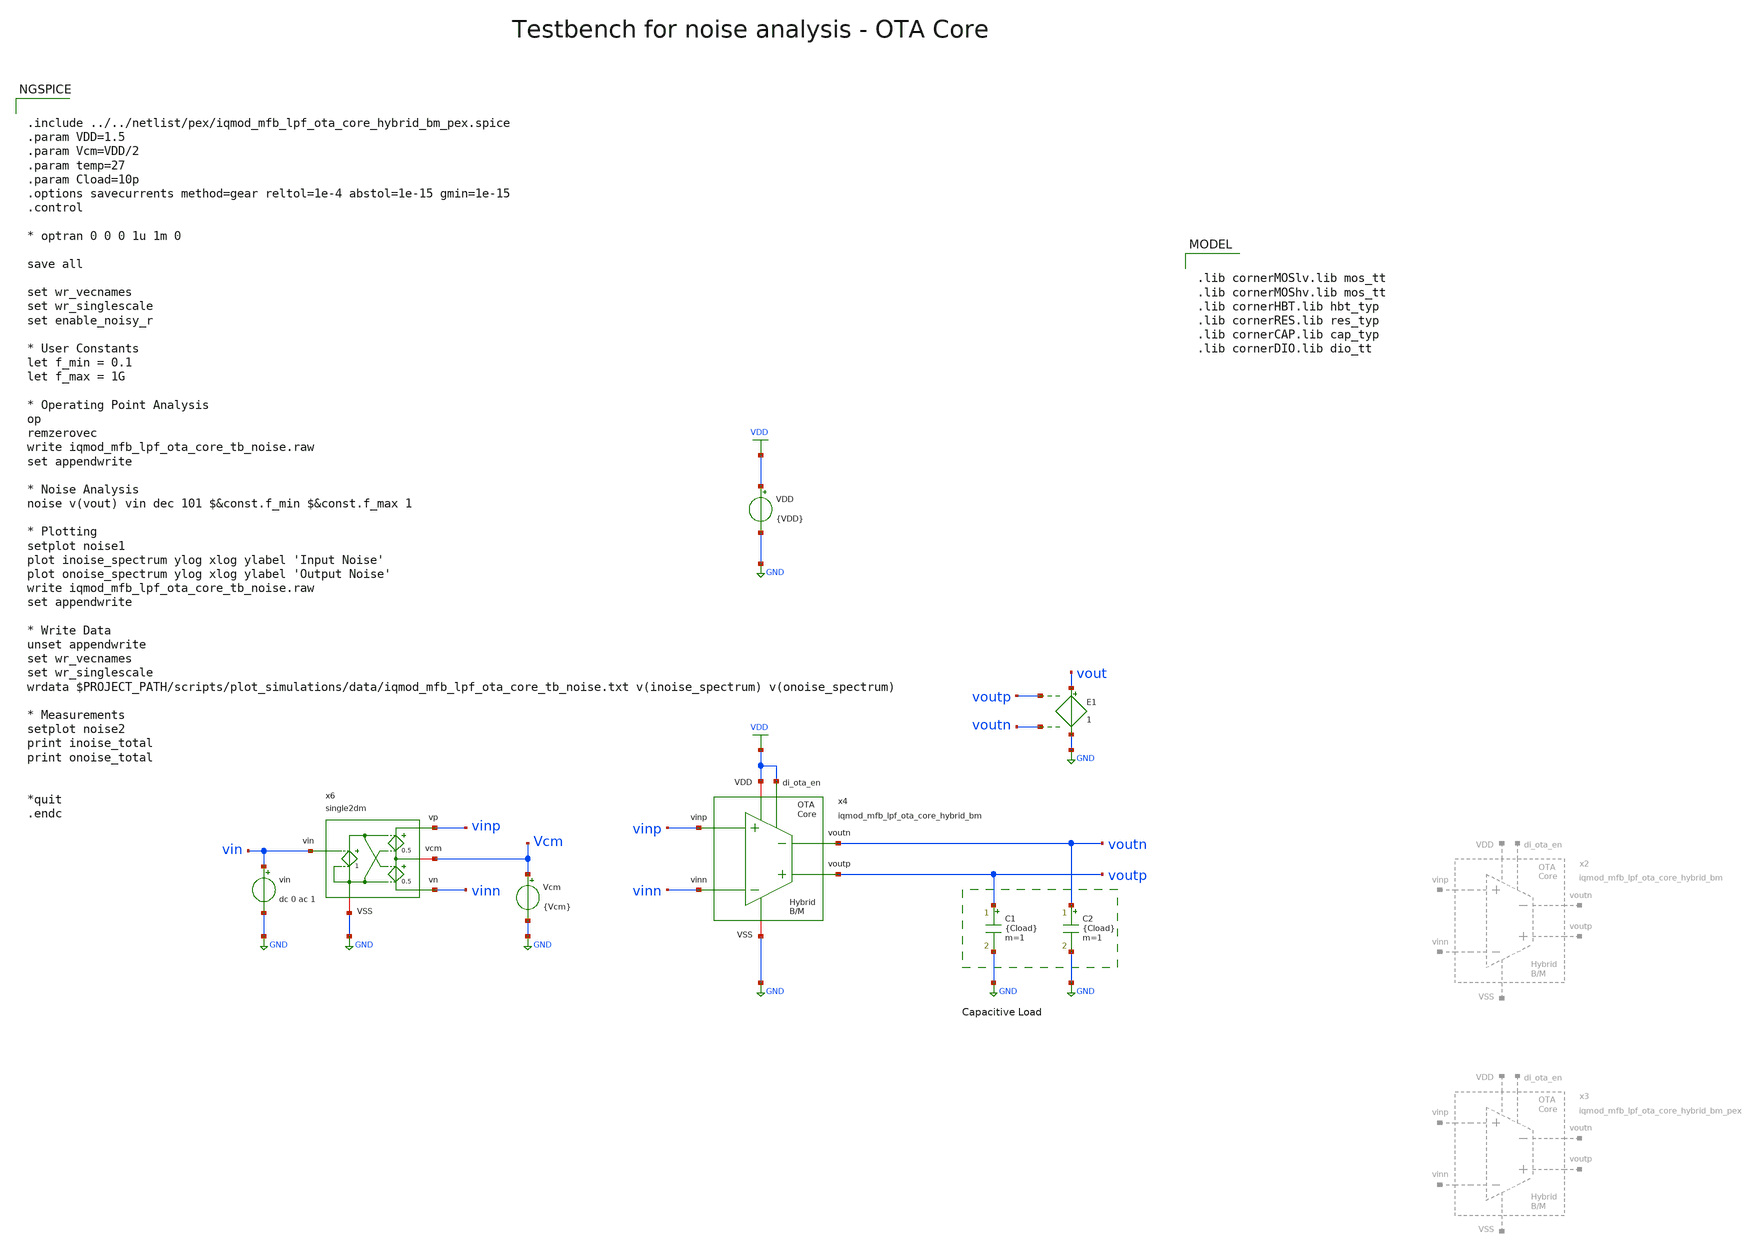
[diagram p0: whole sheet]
** sch_path: ihp130/macros/iqmod/testbenches/iqmod_mfb_lpf_ota_core_tb_noise.sch
**.subckt iqmod_mfb_lpf_ota_core_tb_noise
VDD VDD GND {VDD}
C1 voutp GND {Cload} m=1
C2 voutn GND {Cload} m=1
Vcm Vcm GND {Vcm}
E1 vout GND voutp voutn 1
vin vin GND dc 0 ac 1
x4 voutp voutn vinn vinp VDD GND VDD iqmod_mfb_lpf_ota_core_hybrid_bm
x6 vinp vin Vcm GND vinn single2dm
**** begin user architecture code


.include ../../netlist/pex/iqmod_mfb_lpf_ota_core_hybrid_bm_pex.spice
.param VDD=1.5
.param Vcm=VDD/2
.param temp=27
.param Cload=10p
.options savecurrents method=gear reltol=1e-4 abstol=1e-15 gmin=1e-15
.control

* optran 0 0 0 1u 1m 0

save all

set wr_vecnames
set wr_singlescale
set enable_noisy_r

* User Constants
let f_min = 0.1
let f_max = 1G

* Operating Point Analysis
op
remzerovec
write iqmod_mfb_lpf_ota_core_tb_noise.raw
set appendwrite

* Noise Analysis
noise v(vout) vin dec 101 $&const.f_min $&const.f_max 1

* Plotting
setplot noise1
plot inoise_spectrum ylog xlog ylabel 'Input Noise'
plot onoise_spectrum ylog xlog ylabel 'Output Noise'
write iqmod_mfb_lpf_ota_core_tb_noise.raw
set appendwrite

* Write Data
unset appendwrite
set wr_vecnames
set wr_singlescale
wrdata $PROJECT_PATH/scripts/plot_simulations/data/iqmod_mfb_lpf_ota_core_tb_noise.txt
+ v(inoise_spectrum) v(onoise_spectrum)

* Measurements
setplot noise2
print inoise_total
print onoise_total


*quit
.endc



.lib cornerMOSlv.lib mos_tt
.lib cornerMOShv.lib mos_tt
.lib cornerHBT.lib hbt_typ
.lib cornerRES.lib res_typ
.lib cornerCAP.lib cap_typ
.lib cornerDIO.lib dio_tt

**** end user architecture code
**.ends
.GLOBAL GND
.GLOBAL VDD
.end
